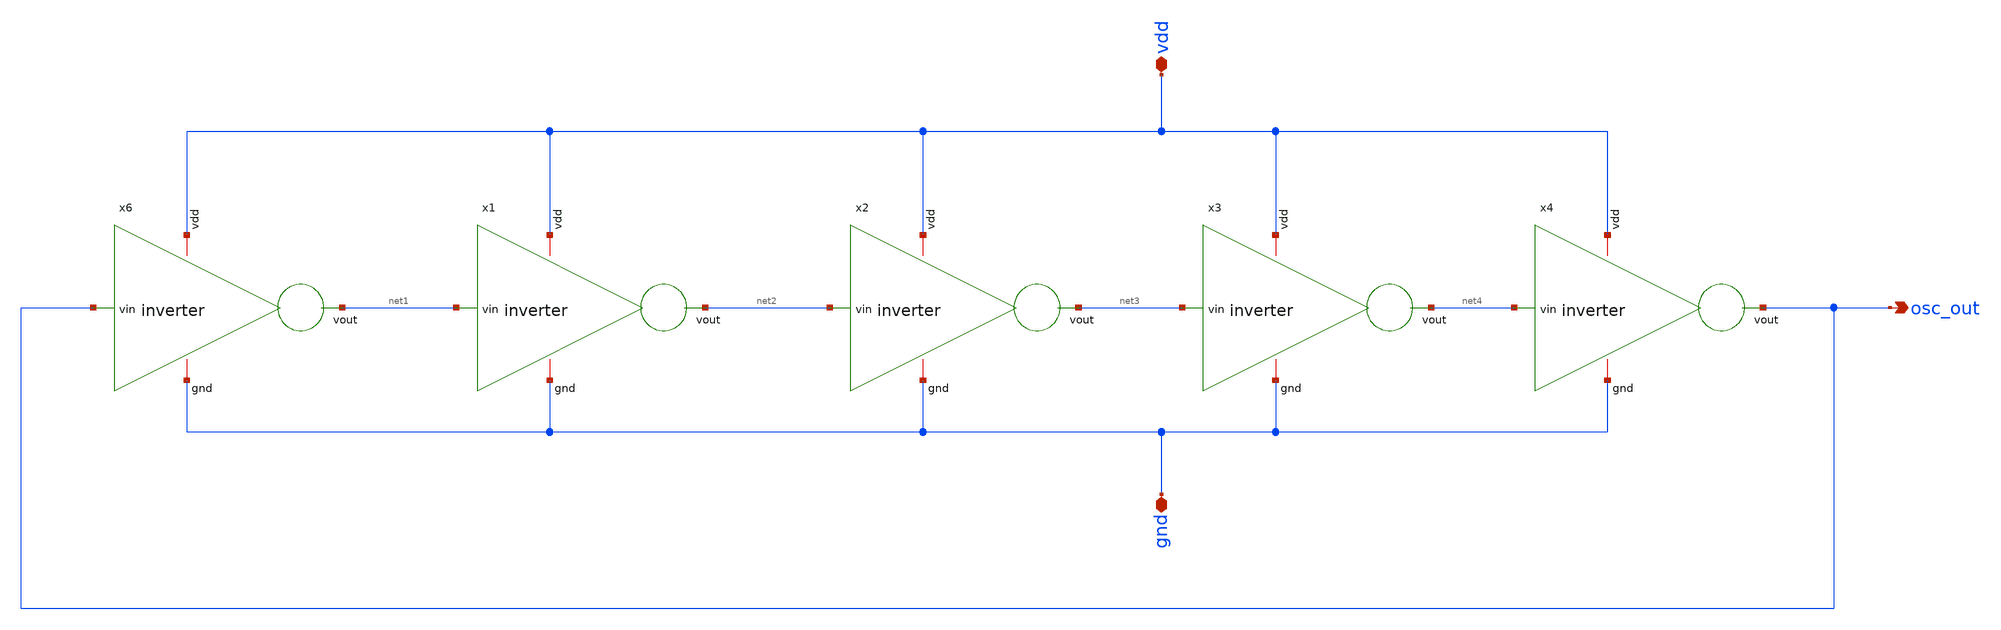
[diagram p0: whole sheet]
** sch_path: design/schematics/sero.sch
**.subckt sero osc_out vdd gnd
*.opin osc_out
*.iopin vdd
*.iopin gnd
x6 vdd osc_out net1 gnd inverter
x1 vdd net1 net2 gnd inverter
x2 vdd net2 net3 gnd inverter
x3 vdd net3 net4 gnd inverter
x4 vdd net4 osc_out gnd inverter
**.ends
.end
